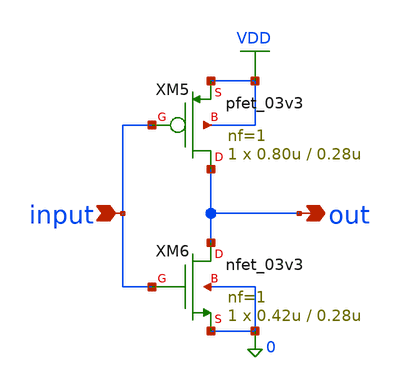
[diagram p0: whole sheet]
** sch_path: xschem/sar_adc/blocks/async_sar/async_inverter.sch
**.subckt async_inverter input out
*.ipin input
*.opin out
XM5 out input VDD VDD pfet_03v3 L=0.28u W=0.80u nf=1 ad='int((nf+1)/2) * W/nf * 0.18u' as='int((nf+2)/2) * W/nf * 0.18u'
+ pd='2*int((nf+1)/2) * (W/nf + 0.18u)' ps='2*int((nf+2)/2) * (W/nf + 0.18u)' nrd='0.18u / W' nrs='0.18u / W'
+ sa=0 sb=0 sd=0 m=1
XM6 out input 0 0 nfet_03v3 L=0.28u W=0.42u nf=1 ad='int((nf+1)/2) * W/nf * 0.18u' as='int((nf+2)/2) * W/nf * 0.18u'
+ pd='2*int((nf+1)/2) * (W/nf + 0.18u)' ps='2*int((nf+2)/2) * (W/nf + 0.18u)' nrd='0.18u / W' nrs='0.18u / W'
+ sa=0 sb=0 sd=0 m=1
**.ends
.GLOBAL VDD
.end
